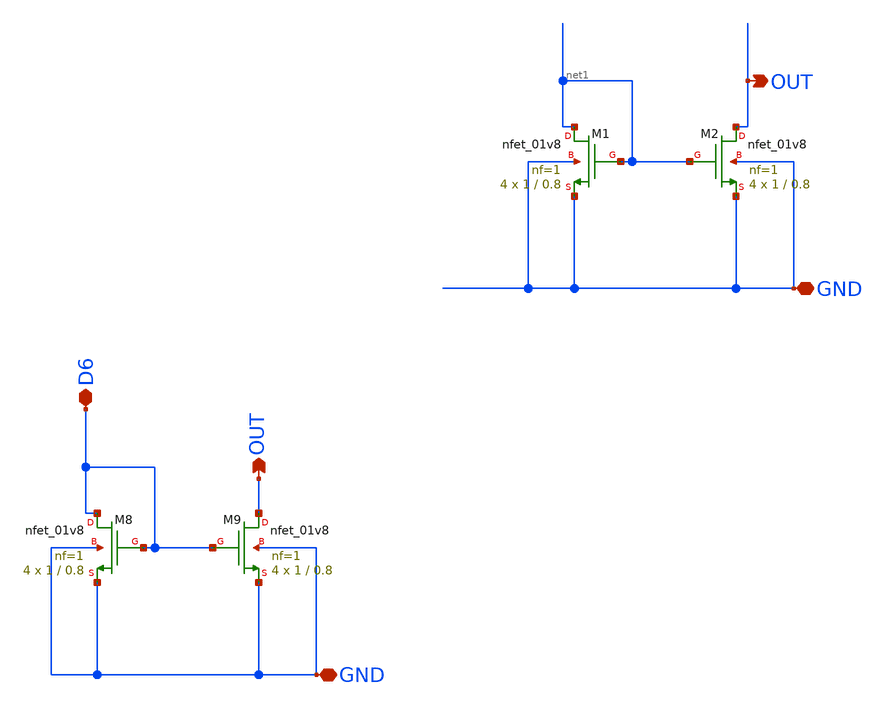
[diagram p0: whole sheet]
** sch_path: OPAMP/mag/untitled.sch
**.subckt untitled GND OUT GND OUT D6
*.iopin GND
*.opin OUT
*.iopin GND
*.opin OUT
*.iopin D6
XM8 D6 D6 GND GND sky130_fd_pr__nfet_01v8 L=0.8 W=1 nf=1 ad='int((nf+1)/2) * W/nf * 0.29' as='int((nf+2)/2) * W/nf * 0.29'
+ pd='2*int((nf+1)/2) * (W/nf + 0.29)' ps='2*int((nf+2)/2) * (W/nf + 0.29)' nrd='0.29 / W' nrs='0.29 / W'
+ sa=0 sb=0 sd=0 mult=4 m=4
XM9 OUT D6 GND GND sky130_fd_pr__nfet_01v8 L=0.8 W=1 nf=1 ad='int((nf+1)/2) * W/nf * 0.29' as='int((nf+2)/2) * W/nf * 0.29'
+ pd='2*int((nf+1)/2) * (W/nf + 0.29)' ps='2*int((nf+2)/2) * (W/nf + 0.29)' nrd='0.29 / W' nrs='0.29 / W'
+ sa=0 sb=0 sd=0 mult=4 m=4
XM1 net1 net1 GND GND sky130_fd_pr__nfet_01v8 L=0.8 W=1 nf=1 ad='int((nf+1)/2) * W/nf * 0.29' as='int((nf+2)/2) * W/nf * 0.29'
+ pd='2*int((nf+1)/2) * (W/nf + 0.29)' ps='2*int((nf+2)/2) * (W/nf + 0.29)' nrd='0.29 / W' nrs='0.29 / W'
+ sa=0 sb=0 sd=0 mult=4 m=4
XM2 OUT net1 GND GND sky130_fd_pr__nfet_01v8 L=0.8 W=1 nf=1 ad='int((nf+1)/2) * W/nf * 0.29' as='int((nf+2)/2) * W/nf * 0.29'
+ pd='2*int((nf+1)/2) * (W/nf + 0.29)' ps='2*int((nf+2)/2) * (W/nf + 0.29)' nrd='0.29 / W' nrs='0.29 / W'
+ sa=0 sb=0 sd=0 mult=4 m=4
**.ends
.end
